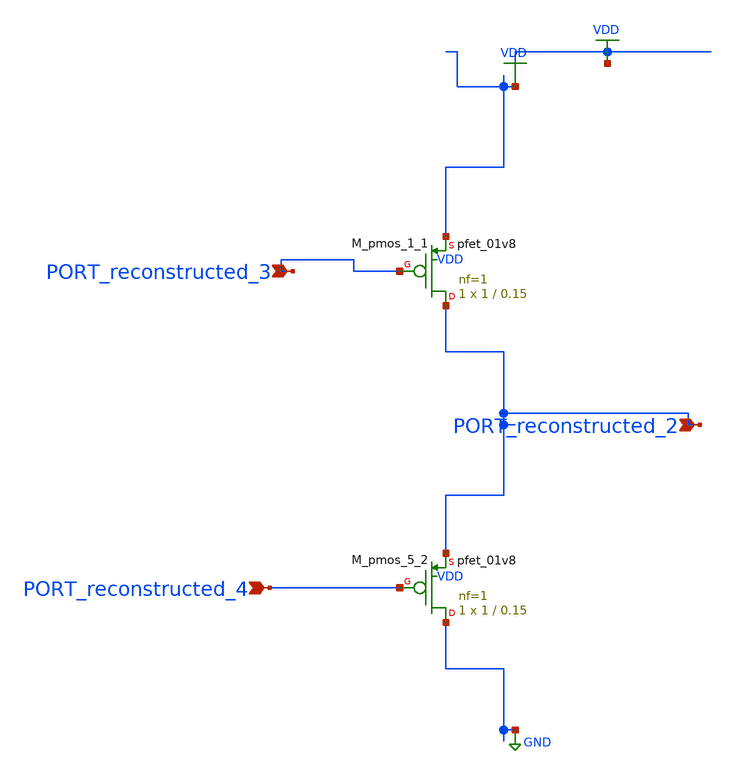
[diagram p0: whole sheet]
** sch_path: schematics/AMSNet/106.sch
**.subckt 106 PORT_reconstructed_3 PORT_reconstructed_2 PORT_reconstructed_4
*.ipin PORT_reconstructed_3
*.ipin PORT_reconstructed_2
*.ipin PORT_reconstructed_4
XM_pmos_1_1 PORT_reconstructed_2 PORT_reconstructed_3 VDD VDD sky130_fd_pr__pfet_01v8 L=0.15 W=1 nf=1
+ ad='int((1 + 1)/2) * 1 / 1 * 0.29' as='int((1 + 2)/2) * 1 / 1 * 0.29' pd='2*int((1 + 1)/2) * (1 / 1 + 0.29)'
+ ps='2*int((1 + 2)/2) * (1 / 1 + 0.29)' nrd='0.29 / 1 ' nrs='0.29 / 1 ' sa=0 sb=0 sd=0 mult=1 m=1
XM_pmos_5_2 GND PORT_reconstructed_4 PORT_reconstructed_2 VDD sky130_fd_pr__pfet_01v8 L=0.15 W=1 nf=1
+ ad='int((1 + 1)/2) * 1 / 1 * 0.29' as='int((1 + 2)/2) * 1 / 1 * 0.29' pd='2*int((1 + 1)/2) * (1 / 1 + 0.29)'
+ ps='2*int((1 + 2)/2) * (1 / 1 + 0.29)' nrd='0.29 / 1 ' nrs='0.29 / 1 ' sa=0 sb=0 sd=0 mult=1 m=1
**.ends
.GLOBAL GND
.GLOBAL VDD
.end
